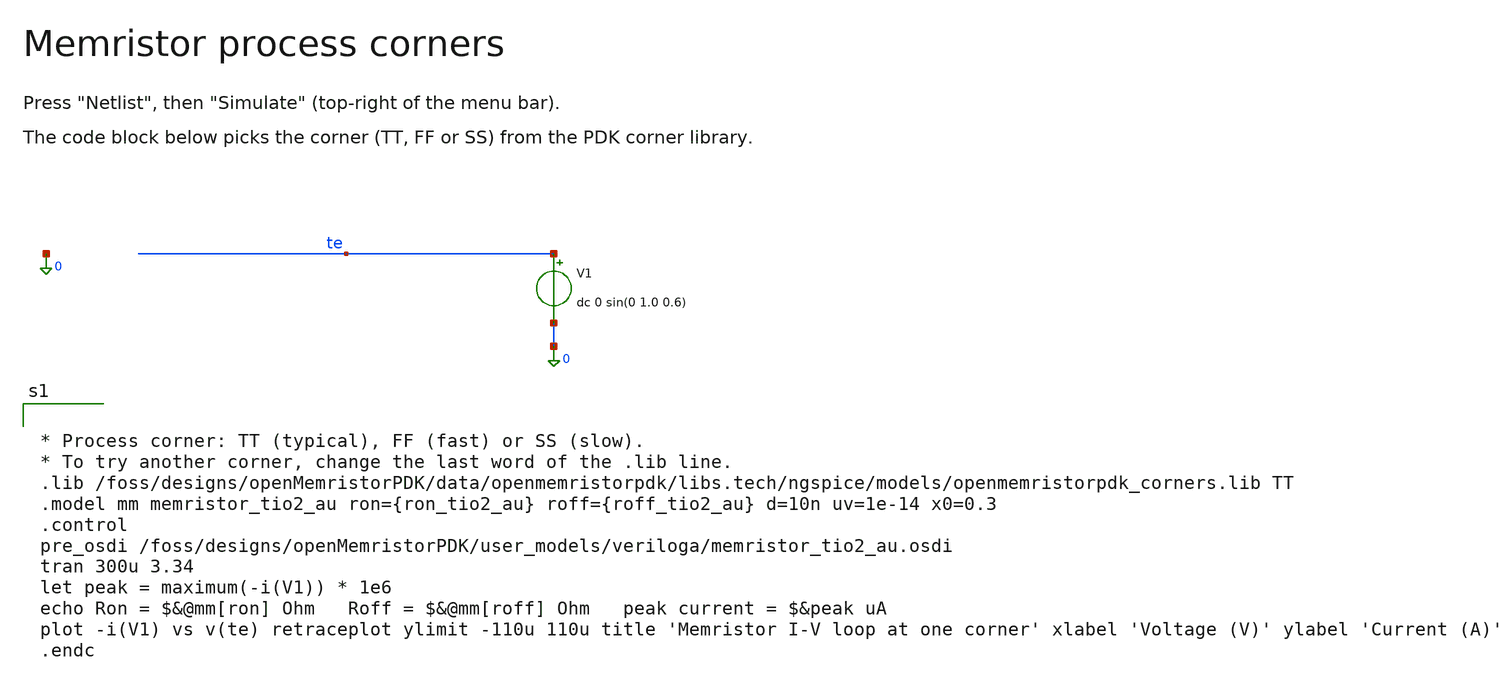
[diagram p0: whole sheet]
** sch_path: libraries/openmemristorpdk_pr/memristor_tio2_au_corners_tb.sch
**.subckt memristor_tio2_au_corners_tb
V1 te 0 dc 0 sin(0 1.0 0.6)
**** begin user architecture code


* Process corner: TT (typical), FF (fast) or SS (slow).
* To try another corner, change the last word of the .lib line.
.lib /foss/designs/openMemristorPDK/data/openmemristorpdk/libs.tech/ngspice/models/openmemristorpdk_corners.lib TT
.model mm memristor_tio2_au ron={ron_tio2_au} roff={roff_tio2_au} d=10n uv=1e-14 x0=0.3
.control
pre_osdi /foss/designs/openMemristorPDK/user_models/veriloga/memristor_tio2_au.osdi
tran 300u 3.34
let peak = maximum(-i(V1)) * 1e6
echo Ron = $&@mm[ron] Ohm   Roff = $&@mm[roff] Ohm   peak current = $&peak uA
plot -i(V1) vs v(te) retraceplot ylimit -110u 110u title 'Memristor I-V loop at one corner' xlabel 'Voltage (V)'
+ ylabel 'Current (A)'
.endc


**** end user architecture code
**.ends
.end
